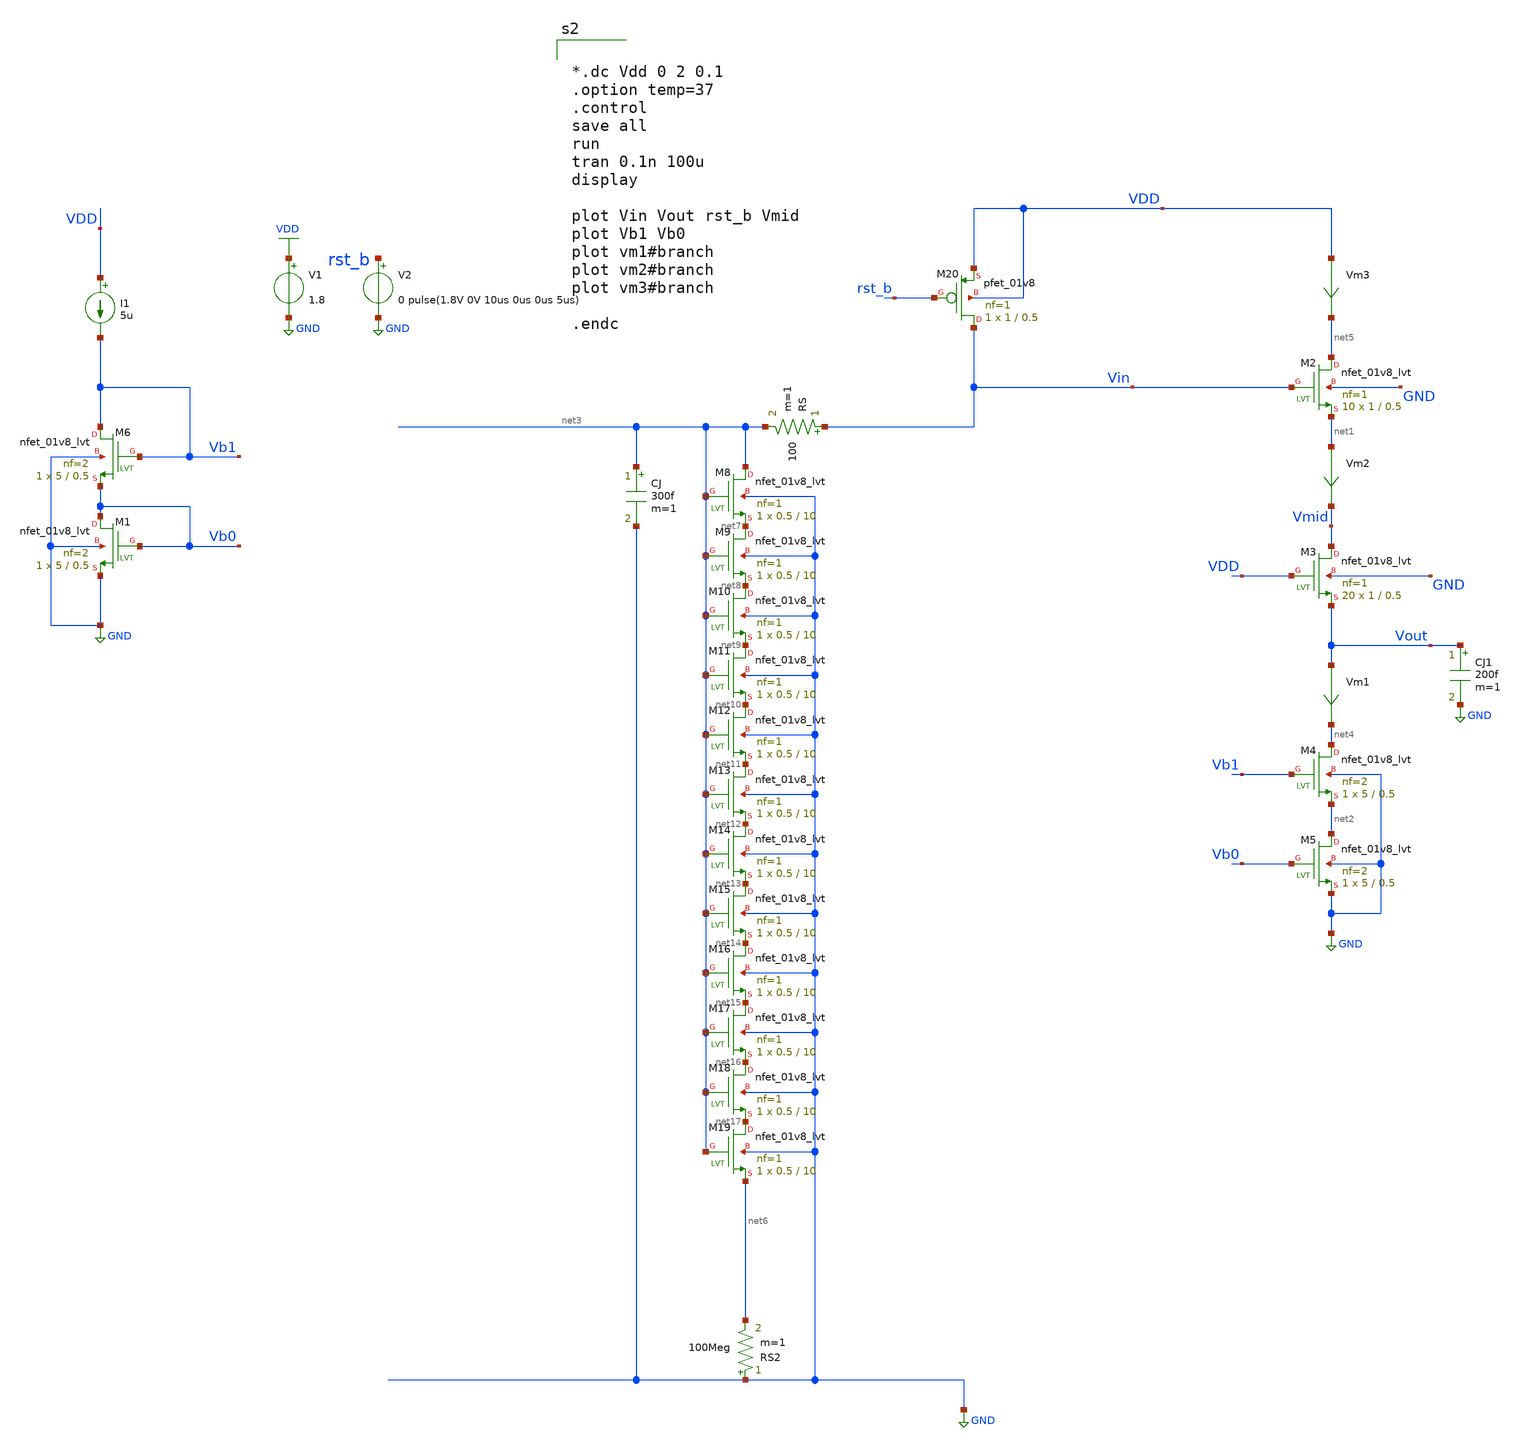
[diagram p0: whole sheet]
** sch_path: xschem/cmos_imager/pixel.sch
**.subckt pixel
XM2 net5 Vin net1 GND sky130_fd_pr__nfet_01v8_lvt L=0.5 W=1 nf=1 ad='int((nf+1)/2) * W/nf * 0.29' as='int((nf+2)/2) * W/nf * 0.29'
+ pd='2*int((nf+1)/2) * (W/nf + 0.29)' ps='2*int((nf+2)/2) * (W/nf + 0.29)' nrd='0.29 / W' nrs='0.29 / W'
+ sa=0 sb=0 sd=0 mult=10 m=10
XM4 net4 Vb1 net2 GND sky130_fd_pr__nfet_01v8_lvt L=0.5 W=5 nf=2 ad='int((nf+1)/2) * W/nf * 0.29' as='int((nf+2)/2) * W/nf * 0.29'
+ pd='2*int((nf+1)/2) * (W/nf + 0.29)' ps='2*int((nf+2)/2) * (W/nf + 0.29)' nrd='0.29 / W' nrs='0.29 / W'
+ sa=0 sb=0 sd=0 mult=1 m=1
XM5 net2 Vb0 GND GND sky130_fd_pr__nfet_01v8_lvt L=0.5 W=5 nf=2 ad='int((nf+1)/2) * W/nf * 0.29' as='int((nf+2)/2) * W/nf * 0.29'
+ pd='2*int((nf+1)/2) * (W/nf + 0.29)' ps='2*int((nf+2)/2) * (W/nf + 0.29)' nrd='0.29 / W' nrs='0.29 / W'
+ sa=0 sb=0 sd=0 mult=1 m=1
CJ net3 GND 300f m=1
RS Vin net3 100 m=1
XM6 Vb1 Vb1 Vb0 GND sky130_fd_pr__nfet_01v8_lvt L=0.5 W=5 nf=2 ad='int((nf+1)/2) * W/nf * 0.29' as='int((nf+2)/2) * W/nf * 0.29'
+ pd='2*int((nf+1)/2) * (W/nf + 0.29)' ps='2*int((nf+2)/2) * (W/nf + 0.29)' nrd='0.29 / W' nrs='0.29 / W'
+ sa=0 sb=0 sd=0 mult=1 m=1
XM1 Vb0 Vb0 GND GND sky130_fd_pr__nfet_01v8_lvt L=0.5 W=5 nf=2 ad='int((nf+1)/2) * W/nf * 0.29' as='int((nf+2)/2) * W/nf * 0.29'
+ pd='2*int((nf+1)/2) * (W/nf + 0.29)' ps='2*int((nf+2)/2) * (W/nf + 0.29)' nrd='0.29 / W' nrs='0.29 / W'
+ sa=0 sb=0 sd=0 mult=1 m=1
I1 VDD Vb1 5u
V1 VDD GND 1.8
Vm1 Vout net4 0
.save i(vm1)
V2 rst_b GND 0 pulse(1.8V 0V 10us 0us 0us 5us)
Vm2 net1 Vmid 0
.save i(vm2)
CJ1 Vout GND 200f m=1
Vm3 VDD net5 0
.save i(vm3)
XM3 Vmid VDD Vout GND sky130_fd_pr__nfet_01v8_lvt L=0.5 W=1 nf=1 ad='int((nf+1)/2) * W/nf * 0.29' as='int((nf+2)/2) * W/nf * 0.29'
+ pd='2*int((nf+1)/2) * (W/nf + 0.29)' ps='2*int((nf+2)/2) * (W/nf + 0.29)' nrd='0.29 / W' nrs='0.29 / W'
+ sa=0 sb=0 sd=0 mult=20 m=20
XM8 net3 net3 net7 GND sky130_fd_pr__nfet_01v8_lvt L=10 W=0.5 nf=1 ad='int((nf+1)/2) * W/nf * 0.29' as='int((nf+2)/2) * W/nf * 0.29'
+ pd='2*int((nf+1)/2) * (W/nf + 0.29)' ps='2*int((nf+2)/2) * (W/nf + 0.29)' nrd='0.29 / W' nrs='0.29 / W'
+ sa=0 sb=0 sd=0 mult=1 m=1
XM9 net7 net3 net8 GND sky130_fd_pr__nfet_01v8_lvt L=10 W=0.5 nf=1 ad='int((nf+1)/2) * W/nf * 0.29' as='int((nf+2)/2) * W/nf * 0.29'
+ pd='2*int((nf+1)/2) * (W/nf + 0.29)' ps='2*int((nf+2)/2) * (W/nf + 0.29)' nrd='0.29 / W' nrs='0.29 / W'
+ sa=0 sb=0 sd=0 mult=1 m=1
XM10 net8 net3 net9 GND sky130_fd_pr__nfet_01v8_lvt L=10 W=0.5 nf=1 ad='int((nf+1)/2) * W/nf * 0.29'
+ as='int((nf+2)/2) * W/nf * 0.29' pd='2*int((nf+1)/2) * (W/nf + 0.29)' ps='2*int((nf+2)/2) * (W/nf + 0.29)'
+ nrd='0.29 / W' nrs='0.29 / W' sa=0 sb=0 sd=0 mult=1 m=1
XM11 net9 net3 net10 GND sky130_fd_pr__nfet_01v8_lvt L=10 W=0.5 nf=1 ad='int((nf+1)/2) * W/nf * 0.29'
+ as='int((nf+2)/2) * W/nf * 0.29' pd='2*int((nf+1)/2) * (W/nf + 0.29)' ps='2*int((nf+2)/2) * (W/nf + 0.29)'
+ nrd='0.29 / W' nrs='0.29 / W' sa=0 sb=0 sd=0 mult=1 m=1
XM12 net10 net3 net11 GND sky130_fd_pr__nfet_01v8_lvt L=10 W=0.5 nf=1 ad='int((nf+1)/2) * W/nf * 0.29'
+ as='int((nf+2)/2) * W/nf * 0.29' pd='2*int((nf+1)/2) * (W/nf + 0.29)' ps='2*int((nf+2)/2) * (W/nf + 0.29)'
+ nrd='0.29 / W' nrs='0.29 / W' sa=0 sb=0 sd=0 mult=1 m=1
XM13 net11 net3 net12 GND sky130_fd_pr__nfet_01v8_lvt L=10 W=0.5 nf=1 ad='int((nf+1)/2) * W/nf * 0.29'
+ as='int((nf+2)/2) * W/nf * 0.29' pd='2*int((nf+1)/2) * (W/nf + 0.29)' ps='2*int((nf+2)/2) * (W/nf + 0.29)'
+ nrd='0.29 / W' nrs='0.29 / W' sa=0 sb=0 sd=0 mult=1 m=1
XM14 net12 net3 net13 GND sky130_fd_pr__nfet_01v8_lvt L=10 W=0.5 nf=1 ad='int((nf+1)/2) * W/nf * 0.29'
+ as='int((nf+2)/2) * W/nf * 0.29' pd='2*int((nf+1)/2) * (W/nf + 0.29)' ps='2*int((nf+2)/2) * (W/nf + 0.29)'
+ nrd='0.29 / W' nrs='0.29 / W' sa=0 sb=0 sd=0 mult=1 m=1
XM15 net13 net3 net14 GND sky130_fd_pr__nfet_01v8_lvt L=10 W=0.5 nf=1 ad='int((nf+1)/2) * W/nf * 0.29'
+ as='int((nf+2)/2) * W/nf * 0.29' pd='2*int((nf+1)/2) * (W/nf + 0.29)' ps='2*int((nf+2)/2) * (W/nf + 0.29)'
+ nrd='0.29 / W' nrs='0.29 / W' sa=0 sb=0 sd=0 mult=1 m=1
XM16 net14 net3 net15 GND sky130_fd_pr__nfet_01v8_lvt L=10 W=0.5 nf=1 ad='int((nf+1)/2) * W/nf * 0.29'
+ as='int((nf+2)/2) * W/nf * 0.29' pd='2*int((nf+1)/2) * (W/nf + 0.29)' ps='2*int((nf+2)/2) * (W/nf + 0.29)'
+ nrd='0.29 / W' nrs='0.29 / W' sa=0 sb=0 sd=0 mult=1 m=1
XM17 net15 net3 net16 GND sky130_fd_pr__nfet_01v8_lvt L=10 W=0.5 nf=1 ad='int((nf+1)/2) * W/nf * 0.29'
+ as='int((nf+2)/2) * W/nf * 0.29' pd='2*int((nf+1)/2) * (W/nf + 0.29)' ps='2*int((nf+2)/2) * (W/nf + 0.29)'
+ nrd='0.29 / W' nrs='0.29 / W' sa=0 sb=0 sd=0 mult=1 m=1
XM18 net16 net3 net17 GND sky130_fd_pr__nfet_01v8_lvt L=10 W=0.5 nf=1 ad='int((nf+1)/2) * W/nf * 0.29'
+ as='int((nf+2)/2) * W/nf * 0.29' pd='2*int((nf+1)/2) * (W/nf + 0.29)' ps='2*int((nf+2)/2) * (W/nf + 0.29)'
+ nrd='0.29 / W' nrs='0.29 / W' sa=0 sb=0 sd=0 mult=1 m=1
XM19 net17 net3 net6 GND sky130_fd_pr__nfet_01v8_lvt L=10 W=0.5 nf=1 ad='int((nf+1)/2) * W/nf * 0.29'
+ as='int((nf+2)/2) * W/nf * 0.29' pd='2*int((nf+1)/2) * (W/nf + 0.29)' ps='2*int((nf+2)/2) * (W/nf + 0.29)'
+ nrd='0.29 / W' nrs='0.29 / W' sa=0 sb=0 sd=0 mult=1 m=1
RS2 GND net6 100Meg m=1
XM20 Vin rst_b VDD VDD sky130_fd_pr__pfet_01v8 L=0.5 W=1 nf=1 ad='int((nf+1)/2) * W/nf * 0.29' as='int((nf+2)/2) * W/nf * 0.29'
+ pd='2*int((nf+1)/2) * (W/nf + 0.29)' ps='2*int((nf+2)/2) * (W/nf + 0.29)' nrd='0.29 / W' nrs='0.29 / W'
+ sa=0 sb=0 sd=0 mult=1 m=1
**** begin user architecture code

** opencircuitdesign pdks install
.lib $::SKYWATER_MODELS/sky130.lib.spice tt




*.dc Vdd 0 2 0.1
.option temp=37
.control
save all
run
tran 0.1n 100u
display

plot Vin Vout rst_b Vmid
plot Vb1 Vb0
plot vm1#branch
plot vm2#branch
plot vm3#branch

.endc


**** end user architecture code
**.ends
.GLOBAL GND
.GLOBAL VDD
.end
